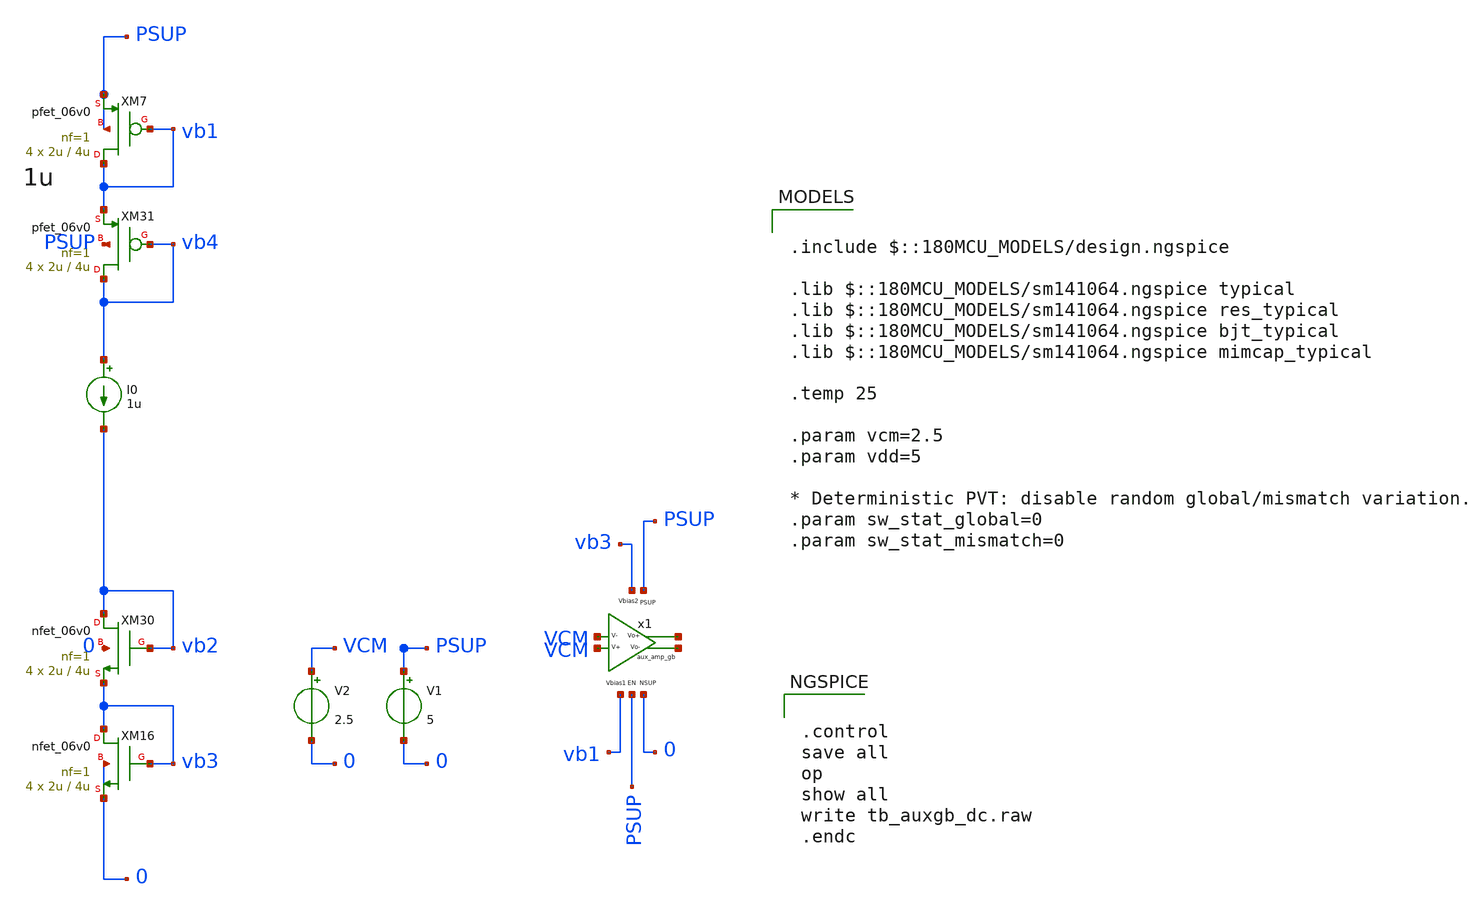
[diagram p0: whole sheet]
** sch_path: xschem/blocks/aux_amp_gb/tb_aux_amp_gb_dc.sch
**.subckt tb_aux_amp_gb_dc
V1 PSUP 0 5
V2 VCM 0 2.5
I0 vb4 vb2 1u
XM7 vb1 vb1 PSUP PSUP pfet_06v0 L=4u W=2u nf=1 ad='int((nf+1)/2) * W/nf * 0.18u' as='int((nf+2)/2) * W/nf * 0.18u'
+ pd='2*int((nf+1)/2) * (W/nf + 0.18u)' ps='2*int((nf+2)/2) * (W/nf + 0.18u)' nrd='0.18u / W' nrs='0.18u / W'
+ sa=0 sb=0 sd=0 m=4
XM16 vb3 vb3 0 0 nfet_06v0 L=4u W=2u nf=1 ad='int((nf+1)/2) * W/nf * 0.18u' as='int((nf+2)/2) * W/nf * 0.18u'
+ pd='2*int((nf+1)/2) * (W/nf + 0.18u)' ps='2*int((nf+2)/2) * (W/nf + 0.18u)' nrd='0.18u / W' nrs='0.18u / W'
+ sa=0 sb=0 sd=0 m=4
XM30 vb2 vb2 vb3 0 nfet_06v0 L=4u W=2u nf=1 ad='int((nf+1)/2) * W/nf * 0.18u' as='int((nf+2)/2) * W/nf * 0.18u'
+ pd='2*int((nf+1)/2) * (W/nf + 0.18u)' ps='2*int((nf+2)/2) * (W/nf + 0.18u)' nrd='0.18u / W' nrs='0.18u / W'
+ sa=0 sb=0 sd=0 m=4
XM31 vb4 vb4 vb1 PSUP pfet_06v0 L=4u W=2u nf=1 ad='int((nf+1)/2) * W/nf * 0.18u' as='int((nf+2)/2) * W/nf * 0.18u'
+ pd='2*int((nf+1)/2) * (W/nf + 0.18u)' ps='2*int((nf+2)/2) * (W/nf + 0.18u)' nrd='0.18u / W' nrs='0.18u / W'
+ sa=0 sb=0 sd=0 m=4
x1 PSUP vb1 VCM VCM vb3 PSUP 0 net1 net2 aux_amp_gb
**** begin user architecture code


.control
save all
op
show all
write tb_auxgb_dc.raw
.endc



.include $::180MCU_MODELS/design.ngspice

.lib $::180MCU_MODELS/sm141064.ngspice typical
.lib $::180MCU_MODELS/sm141064.ngspice res_typical
.lib $::180MCU_MODELS/sm141064.ngspice bjt_typical
.lib $::180MCU_MODELS/sm141064.ngspice mimcap_typical

.temp 25

.param vcm=2.5
.param vdd=5

* Deterministic PVT: disable random global/mismatch variation.
.param sw_stat_global=0
.param sw_stat_mismatch=0


**** end user architecture code
**.ends

* expanding   symbol:  blocks/aux_amp_gb/aux_amp_gb.sym # of pins=9
** sym_path: xschem/blocks/aux_amp_gb/aux_amp_gb.sym
** sch_path: xschem/blocks/aux_amp_gb/aux_amp_gb.sch
.subckt aux_amp_gb PSUP Vbias1 V- V+ Vbias2 EN NSUP Vo+ Vo-
*.ipin PSUP
*.ipin NSUP
*.ipin EN
*.opin Vo-
*.ipin V+
*.ipin V-
*.opin Vo+
*.ipin Vbias1
*.ipin Vbias2
XM9 Vo- V+ n2 NSUP nfet_06v0 L=2u W=4u nf=5 ad='int((nf+1)/2) * W/nf * 0.18u' as='int((nf+2)/2) * W/nf * 0.18u'
+ pd='2*int((nf+1)/2) * (W/nf + 0.18u)' ps='2*int((nf+2)/2) * (W/nf + 0.18u)' nrd='0.18u / W' nrs='0.18u / W'
+ sa=0 sb=0 sd=0 m=4
XM10 Vo+ V- n2 NSUP nfet_06v0 L=2u W=4u nf=5 ad='int((nf+1)/2) * W/nf * 0.18u' as='int((nf+2)/2) * W/nf * 0.18u'
+ pd='2*int((nf+1)/2) * (W/nf + 0.18u)' ps='2*int((nf+2)/2) * (W/nf + 0.18u)' nrd='0.18u / W' nrs='0.18u / W'
+ sa=0 sb=0 sd=0 m=4
XM11 Vo- Vbias1 PSUP PSUP pfet_06v0 L=4u W=2u nf=1 ad='int((nf+1)/2) * W/nf * 0.18u' as='int((nf+2)/2) * W/nf * 0.18u'
+ pd='2*int((nf+1)/2) * (W/nf + 0.18u)' ps='2*int((nf+2)/2) * (W/nf + 0.18u)' nrd='0.18u / W' nrs='0.18u / W'
+ sa=0 sb=0 sd=0 m=4
XM12 Vo+ Vbias1 PSUP PSUP pfet_06v0 L=4u W=2u nf=1 ad='int((nf+1)/2) * W/nf * 0.18u' as='int((nf+2)/2) * W/nf * 0.18u'
+ pd='2*int((nf+1)/2) * (W/nf + 0.18u)' ps='2*int((nf+2)/2) * (W/nf + 0.18u)' nrd='0.18u / W' nrs='0.18u / W'
+ sa=0 sb=0 sd=0 m=4
XM15 n2 Vbias2 NSUP NSUP nfet_06v0 L=4u W=2u nf=1 ad='int((nf+1)/2) * W/nf * 0.18u' as='int((nf+2)/2) * W/nf * 0.18u'
+ pd='2*int((nf+1)/2) * (W/nf + 0.18u)' ps='2*int((nf+2)/2) * (W/nf + 0.18u)' nrd='0.18u / W' nrs='0.18u / W'
+ sa=0 sb=0 sd=0 m=8
.ends

.end
